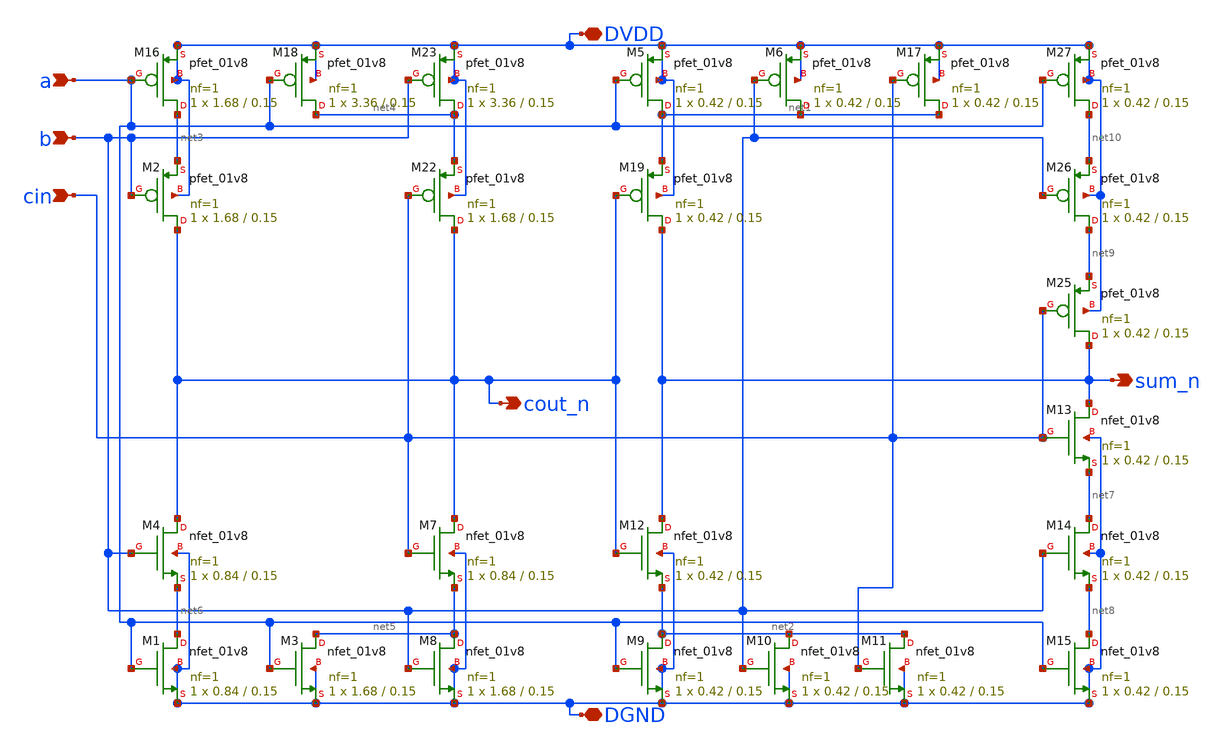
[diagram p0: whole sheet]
** sch_path: tut6/sim/pre_layout/fa.sch
**.subckt fa DVDD DGND sum_n cout_n a b cin
*.iopin DVDD
*.iopin DGND
*.opin sum_n
*.opin cout_n
*.ipin a
*.ipin b
*.ipin cin
XM3 net5 a DGND DGND sky130_fd_pr__nfet_01v8 L=0.15 W=1.68 nf=1 ad='int((nf+1)/2) * W/nf * 0.29' as='int((nf+2)/2) * W/nf * 0.29'
+ pd='2*int((nf+1)/2) * (W/nf + 0.29)' ps='2*int((nf+2)/2) * (W/nf + 0.29)' nrd='0.29 / W' nrs='0.29 / W'
+ sa=0 sb=0 sd=0 mult=1 m=1
XM7 cout_n cin net5 DGND sky130_fd_pr__nfet_01v8 L=0.15 W=0.84 nf=1 ad='int((nf+1)/2) * W/nf * 0.29'
+ as='int((nf+2)/2) * W/nf * 0.29' pd='2*int((nf+1)/2) * (W/nf + 0.29)' ps='2*int((nf+2)/2) * (W/nf + 0.29)'
+ nrd='0.29 / W' nrs='0.29 / W' sa=0 sb=0 sd=0 mult=1 m=1
XM8 net5 b DGND DGND sky130_fd_pr__nfet_01v8 L=0.15 W=1.68 nf=1 ad='int((nf+1)/2) * W/nf * 0.29' as='int((nf+2)/2) * W/nf * 0.29'
+ pd='2*int((nf+1)/2) * (W/nf + 0.29)' ps='2*int((nf+2)/2) * (W/nf + 0.29)' nrd='0.29 / W' nrs='0.29 / W'
+ sa=0 sb=0 sd=0 mult=1 m=1
XM9 net2 a DGND DGND sky130_fd_pr__nfet_01v8 L=0.15 W=0.42 nf=1 ad='int((nf+1)/2) * W/nf * 0.29' as='int((nf+2)/2) * W/nf * 0.29'
+ pd='2*int((nf+1)/2) * (W/nf + 0.29)' ps='2*int((nf+2)/2) * (W/nf + 0.29)' nrd='0.29 / W' nrs='0.29 / W'
+ sa=0 sb=0 sd=0 mult=1 m=1
XM10 net2 b DGND DGND sky130_fd_pr__nfet_01v8 L=0.15 W=0.42 nf=1 ad='int((nf+1)/2) * W/nf * 0.29' as='int((nf+2)/2) * W/nf * 0.29'
+ pd='2*int((nf+1)/2) * (W/nf + 0.29)' ps='2*int((nf+2)/2) * (W/nf + 0.29)' nrd='0.29 / W' nrs='0.29 / W'
+ sa=0 sb=0 sd=0 mult=1 m=1
XM11 net2 cin DGND DGND sky130_fd_pr__nfet_01v8 L=0.15 W=0.42 nf=1 ad='int((nf+1)/2) * W/nf * 0.29' as='int((nf+2)/2) * W/nf * 0.29'
+ pd='2*int((nf+1)/2) * (W/nf + 0.29)' ps='2*int((nf+2)/2) * (W/nf + 0.29)' nrd='0.29 / W' nrs='0.29 / W'
+ sa=0 sb=0 sd=0 mult=1 m=1
XM12 sum_n cout_n net2 DGND sky130_fd_pr__nfet_01v8 L=0.15 W=0.42 nf=1 ad='int((nf+1)/2) * W/nf * 0.29'
+ as='int((nf+2)/2) * W/nf * 0.29' pd='2*int((nf+1)/2) * (W/nf + 0.29)' ps='2*int((nf+2)/2) * (W/nf + 0.29)'
+ nrd='0.29 / W' nrs='0.29 / W' sa=0 sb=0 sd=0 mult=1 m=1
XM13 sum_n cin net7 DGND sky130_fd_pr__nfet_01v8 L=0.15 W=0.42 nf=1 ad='int((nf+1)/2) * W/nf * 0.29'
+ as='int((nf+2)/2) * W/nf * 0.29' pd='2*int((nf+1)/2) * (W/nf + 0.29)' ps='2*int((nf+2)/2) * (W/nf + 0.29)'
+ nrd='0.29 / W' nrs='0.29 / W' sa=0 sb=0 sd=0 mult=1 m=1
XM14 net7 b net8 DGND sky130_fd_pr__nfet_01v8 L=0.15 W=0.42 nf=1 ad='int((nf+1)/2) * W/nf * 0.29' as='int((nf+2)/2) * W/nf * 0.29'
+ pd='2*int((nf+1)/2) * (W/nf + 0.29)' ps='2*int((nf+2)/2) * (W/nf + 0.29)' nrd='0.29 / W' nrs='0.29 / W'
+ sa=0 sb=0 sd=0 mult=1 m=1
XM15 net8 a DGND DGND sky130_fd_pr__nfet_01v8 L=0.15 W=0.42 nf=1 ad='int((nf+1)/2) * W/nf * 0.29' as='int((nf+2)/2) * W/nf * 0.29'
+ pd='2*int((nf+1)/2) * (W/nf + 0.29)' ps='2*int((nf+2)/2) * (W/nf + 0.29)' nrd='0.29 / W' nrs='0.29 / W'
+ sa=0 sb=0 sd=0 mult=1 m=1
XM16 net3 a DVDD DVDD sky130_fd_pr__pfet_01v8 L=0.15 W=1.68 nf=1 ad='int((nf+1)/2) * W/nf * 0.29' as='int((nf+2)/2) * W/nf * 0.29'
+ pd='2*int((nf+1)/2) * (W/nf + 0.29)' ps='2*int((nf+2)/2) * (W/nf + 0.29)' nrd='0.29 / W' nrs='0.29 / W'
+ sa=0 sb=0 sd=0 mult=1 m=1
XM18 net4 a DVDD DVDD sky130_fd_pr__pfet_01v8 L=0.15 W=3.36 nf=1 ad='int((nf+1)/2) * W/nf * 0.29' as='int((nf+2)/2) * W/nf * 0.29'
+ pd='2*int((nf+1)/2) * (W/nf + 0.29)' ps='2*int((nf+2)/2) * (W/nf + 0.29)' nrd='0.29 / W' nrs='0.29 / W'
+ sa=0 sb=0 sd=0 mult=1 m=1
XM22 cout_n cin net4 DVDD sky130_fd_pr__pfet_01v8 L=0.15 W=1.68 nf=1 ad='int((nf+1)/2) * W/nf * 0.29'
+ as='int((nf+2)/2) * W/nf * 0.29' pd='2*int((nf+1)/2) * (W/nf + 0.29)' ps='2*int((nf+2)/2) * (W/nf + 0.29)'
+ nrd='0.29 / W' nrs='0.29 / W' sa=0 sb=0 sd=0 mult=1 m=1
XM23 net4 b DVDD DVDD sky130_fd_pr__pfet_01v8 L=0.15 W=3.36 nf=1 ad='int((nf+1)/2) * W/nf * 0.29' as='int((nf+2)/2) * W/nf * 0.29'
+ pd='2*int((nf+1)/2) * (W/nf + 0.29)' ps='2*int((nf+2)/2) * (W/nf + 0.29)' nrd='0.29 / W' nrs='0.29 / W'
+ sa=0 sb=0 sd=0 mult=1 m=1
XM25 sum_n cin net9 DVDD sky130_fd_pr__pfet_01v8 L=0.15 W=0.42 nf=1 ad='int((nf+1)/2) * W/nf * 0.29'
+ as='int((nf+2)/2) * W/nf * 0.29' pd='2*int((nf+1)/2) * (W/nf + 0.29)' ps='2*int((nf+2)/2) * (W/nf + 0.29)'
+ nrd='0.29 / W' nrs='0.29 / W' sa=0 sb=0 sd=0 mult=1 m=1
XM26 net9 b net10 DVDD sky130_fd_pr__pfet_01v8 L=0.15 W=0.42 nf=1 ad='int((nf+1)/2) * W/nf * 0.29' as='int((nf+2)/2) * W/nf * 0.29'
+ pd='2*int((nf+1)/2) * (W/nf + 0.29)' ps='2*int((nf+2)/2) * (W/nf + 0.29)' nrd='0.29 / W' nrs='0.29 / W'
+ sa=0 sb=0 sd=0 mult=1 m=1
XM27 net10 a DVDD DVDD sky130_fd_pr__pfet_01v8 L=0.15 W=0.42 nf=1 ad='int((nf+1)/2) * W/nf * 0.29' as='int((nf+2)/2) * W/nf * 0.29'
+ pd='2*int((nf+1)/2) * (W/nf + 0.29)' ps='2*int((nf+2)/2) * (W/nf + 0.29)' nrd='0.29 / W' nrs='0.29 / W'
+ sa=0 sb=0 sd=0 mult=1 m=1
XM1 net6 a DGND DGND sky130_fd_pr__nfet_01v8 L=0.15 W=0.84 nf=1 ad='int((nf+1)/2) * W/nf * 0.29' as='int((nf+2)/2) * W/nf * 0.29'
+ pd='2*int((nf+1)/2) * (W/nf + 0.29)' ps='2*int((nf+2)/2) * (W/nf + 0.29)' nrd='0.29 / W' nrs='0.29 / W'
+ sa=0 sb=0 sd=0 mult=1 m=1
XM2 cout_n b net3 DVDD sky130_fd_pr__pfet_01v8 L=0.15 W=1.68 nf=1 ad='int((nf+1)/2) * W/nf * 0.29' as='int((nf+2)/2) * W/nf * 0.29'
+ pd='2*int((nf+1)/2) * (W/nf + 0.29)' ps='2*int((nf+2)/2) * (W/nf + 0.29)' nrd='0.29 / W' nrs='0.29 / W'
+ sa=0 sb=0 sd=0 mult=1 m=1
XM4 cout_n b net6 DGND sky130_fd_pr__nfet_01v8 L=0.15 W=0.84 nf=1 ad='int((nf+1)/2) * W/nf * 0.29' as='int((nf+2)/2) * W/nf * 0.29'
+ pd='2*int((nf+1)/2) * (W/nf + 0.29)' ps='2*int((nf+2)/2) * (W/nf + 0.29)' nrd='0.29 / W' nrs='0.29 / W'
+ sa=0 sb=0 sd=0 mult=1 m=1
XM5 net1 a DVDD DVDD sky130_fd_pr__pfet_01v8 L=0.15 W=0.42 nf=1 ad='int((nf+1)/2) * W/nf * 0.29' as='int((nf+2)/2) * W/nf * 0.29'
+ pd='2*int((nf+1)/2) * (W/nf + 0.29)' ps='2*int((nf+2)/2) * (W/nf + 0.29)' nrd='0.29 / W' nrs='0.29 / W'
+ sa=0 sb=0 sd=0 mult=1 m=1
XM6 net1 b DVDD DVDD sky130_fd_pr__pfet_01v8 L=0.15 W=0.42 nf=1 ad='int((nf+1)/2) * W/nf * 0.29' as='int((nf+2)/2) * W/nf * 0.29'
+ pd='2*int((nf+1)/2) * (W/nf + 0.29)' ps='2*int((nf+2)/2) * (W/nf + 0.29)' nrd='0.29 / W' nrs='0.29 / W'
+ sa=0 sb=0 sd=0 mult=1 m=1
XM17 net1 cin DVDD DVDD sky130_fd_pr__pfet_01v8 L=0.15 W=0.42 nf=1 ad='int((nf+1)/2) * W/nf * 0.29' as='int((nf+2)/2) * W/nf * 0.29'
+ pd='2*int((nf+1)/2) * (W/nf + 0.29)' ps='2*int((nf+2)/2) * (W/nf + 0.29)' nrd='0.29 / W' nrs='0.29 / W'
+ sa=0 sb=0 sd=0 mult=1 m=1
XM19 sum_n cout_n net1 DVDD sky130_fd_pr__pfet_01v8 L=0.15 W=0.42 nf=1 ad='int((nf+1)/2) * W/nf * 0.29'
+ as='int((nf+2)/2) * W/nf * 0.29' pd='2*int((nf+1)/2) * (W/nf + 0.29)' ps='2*int((nf+2)/2) * (W/nf + 0.29)'
+ nrd='0.29 / W' nrs='0.29 / W' sa=0 sb=0 sd=0 mult=1 m=1
**.ends
.end
